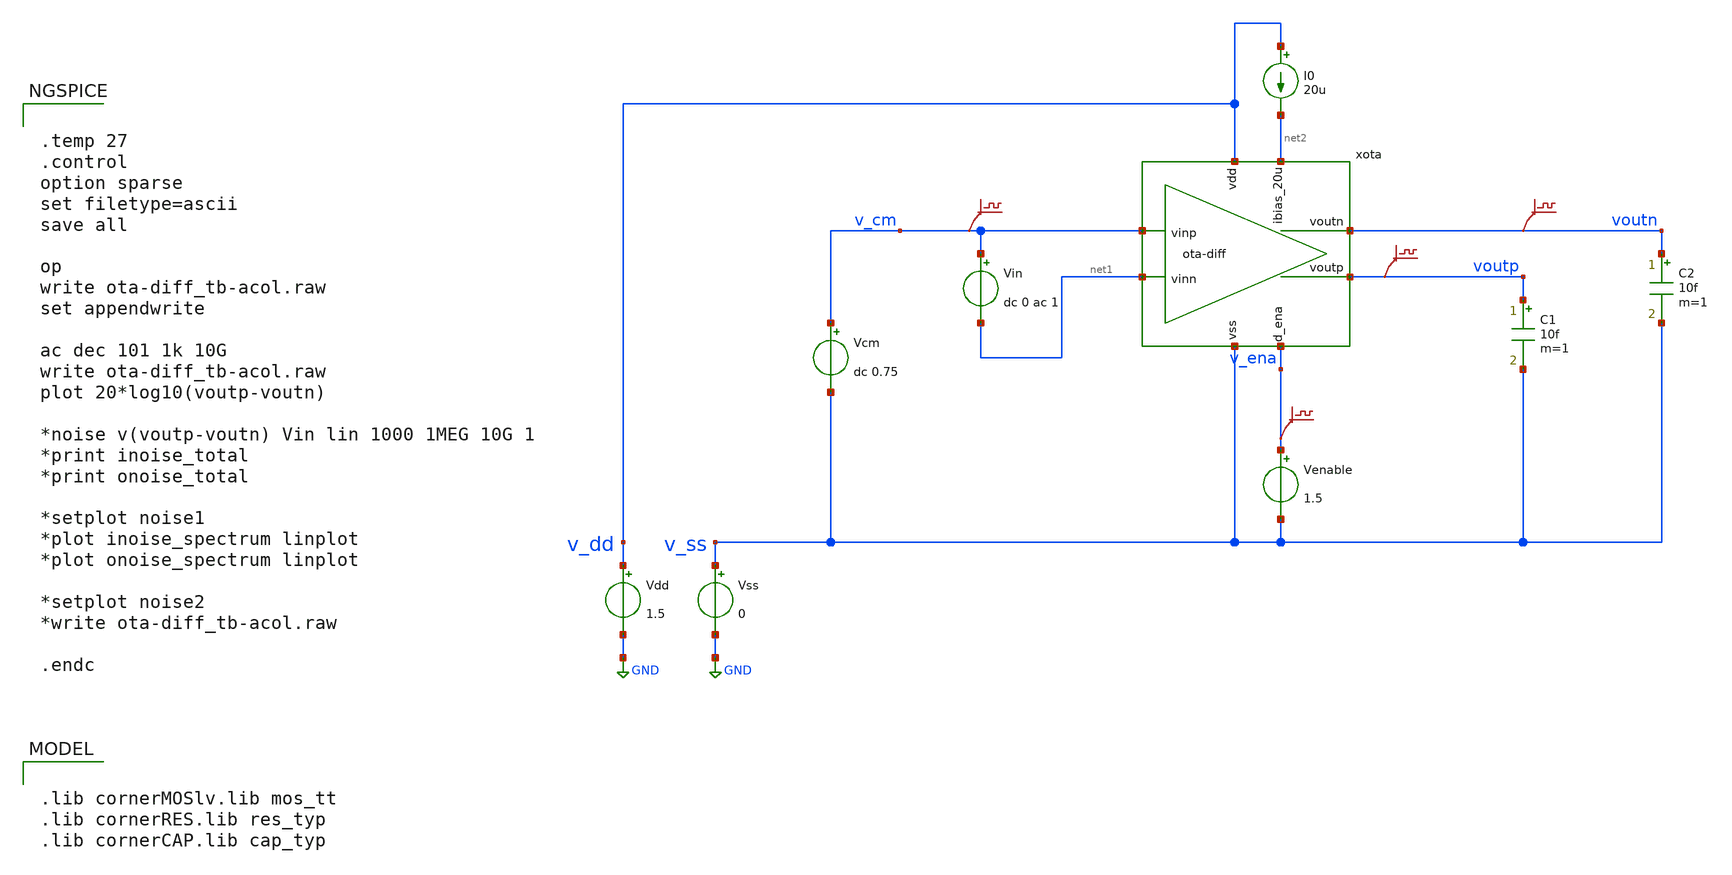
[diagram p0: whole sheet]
** sch_path: xschem/ota-diff_tb-acol.sch
* (c) 2024-2025 H. Pretl, Apache-2.0 license
* xschem/ota-diff.sch:
* (c) 2025 H. Pretl, Apache-2.0 license
**.subckt ota-diff_tb-acol
Vdd v_dd GND 1.5
xota v_dd v_cm net1 net2 v_ena v_ss voutn voutp ota-diff
Vss v_ss GND 0
C1 voutp v_ss 10f m=1
Vcm v_cm v_ss dc 0.75
I0 v_dd net2 20u
Venable v_ena v_ss 1.5
.save v(v_cm)
.save v(voutp)
.save v(v_ena)
Vin v_cm net1 dc 0 ac 1
C2 voutn v_ss 10f m=1
.save v(voutn)
**** begin user architecture code

.lib cornerMOSlv.lib mos_tt
.lib cornerRES.lib res_typ
.lib cornerCAP.lib cap_typ



.temp 27
.control
option sparse
set filetype=ascii
save all

op
write ota-diff_tb-acol.raw
set appendwrite

ac dec 101 1k 10G
write ota-diff_tb-acol.raw
plot 20*log10(voutp-voutn)

*noise v(voutp-voutn) Vin lin 1000 1MEG 10G 1
*print inoise_total
*print onoise_total

*setplot noise1
*plot inoise_spectrum linplot
*plot onoise_spectrum linplot

*setplot noise2
*write ota-diff_tb-acol.raw

.endc


**** end user architecture code
**.ends

* expanding   symbol:  ota-diff.sym # of pins=8
** sym_path: xschem/ota-diff.sym
** sch_path: xschem/ota-diff.sch
.subckt ota-diff vdd vinp vinn ibias_20u d_ena vss voutn voutp
*.ipin ibias_20u
*.iopin vdd
*.iopin vss
*.ipin vinp
*.ipin vinn
*.opin voutp
*.ipin d_ena
*.opin voutn
XM10 vss gate_n net7 vss sg13_lv_nmos w=50u l=5u ng=10 m=1 mm_ok=1
XM1 tail vinp vintn vss sg13_lv_nmos w=10u l=0.5u ng=2 m=1 mm_ok=1
XM2 tail vinn vintp vss sg13_lv_nmos w=10u l=0.5u ng=2 m=1 mm_ok=1
XM3 vintn gate_p vdd vdd sg13_lv_pmos w=10u l=0.5u ng=2 m=1 mm_ok=1
XM9 vss gate_n ibias_20u vss sg13_lv_nmos w=5u l=5u ng=1 m=1 mm_ok=1
XM16 vss ena_n gate_n vss sg13_lv_nmos w=5u l=0.13u ng=1 m=1 mm_ok=1
XM18 gate_p ena vdd vdd sg13_lv_pmos w=5u l=0.13u ng=1 m=1 mm_ok=1
XM14 vss ena_n ena vss sg13_lv_nmos w=5u l=0.13u ng=1 m=1 mm_ok=1
XM15 ena ena_n vdd vdd sg13_lv_pmos w=5u l=0.13u ng=1 m=1 mm_ok=1
XM17 gate_n ena ibias_20u vss sg13_lv_nmos w=5u l=0.13u ng=1 m=1 mm_ok=1
XM12 vss d_ena ena_n vss sg13_lv_nmos w=5u l=0.13u ng=1 m=1 mm_ok=1
XM13 ena_n d_ena vdd vdd sg13_lv_pmos w=5u l=0.13u ng=1 m=1 mm_ok=1
XM7 vss net1 voutp vss sg13_lv_nmos w=20u l=5u ng=4 m=1 mm_ok=1
XR1 gate_p vintn sub! rhigh w=0.5e-6 l=35e-6 m=1 b=0 mm_ok=1
XR3 net1 voutp sub! rhigh w=0.5e-6 l=60e-6 m=1 b=0 mm_ok=1
XM11_1 net6 gate_n net8 vss sg13_lv_nmos w=1u l=5u ng=1 m=1 mm_ok=1
XRM1 vintn net3 sub! rhigh w=0.5e-6 l=2e-6 m=1 b=0 mm_ok=1
XCM1 net3 net2 cap_cmim w=8.0e-6 l=8.0e-6 m=1 mm_ok=1
XM5 vintp gate_p vdd vdd sg13_lv_pmos w=10u l=0.5u ng=2 m=1 mm_ok=1
XM4 net2 vintn vdd vdd sg13_lv_pmos w=10u l=0.5u ng=2 m=1 mm_ok=1
XM6 net4 vintp vdd vdd sg13_lv_pmos w=10u l=0.5u ng=2 m=1 mm_ok=1
XR2 gate_p vintp sub! rhigh w=0.5e-6 l=35e-6 m=1 b=0 mm_ok=1
XRM2 vintp net5 sub! rhigh w=0.5e-6 l=2e-6 m=1 b=0 mm_ok=1
XCM2 net5 net4 cap_cmim w=8.0e-6 l=8.0e-6 m=1 mm_ok=1
XM8 vss net1 voutn vss sg13_lv_nmos w=20u l=5u ng=4 m=1 mm_ok=1
XM11_2 vss gate_n net6 vss sg13_lv_nmos w=1u l=5u ng=1 m=1 mm_ok=1
XR4 net1 voutn sub! rhigh w=0.5e-6 l=60e-6 m=1 b=0 mm_ok=1
Vmeas tail net7 0
.save i(vmeas)
Vmeas1 net2 voutp 0
.save i(vmeas1)
Vmeas2 net4 voutn 0
.save i(vmeas2)
Vmeas3 net1 net8 0
.save i(vmeas3)
.ends

.GLOBAL GND
.end
